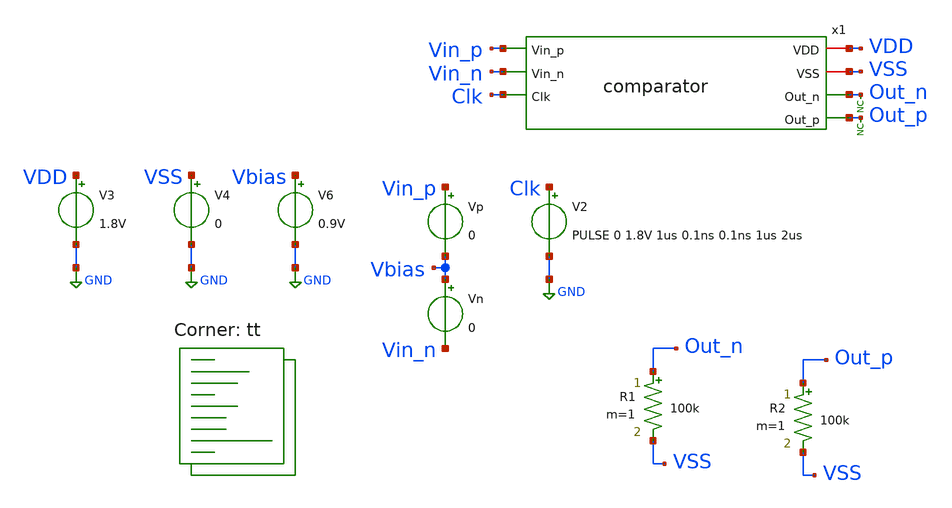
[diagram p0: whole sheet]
** sch_path: xschem/tests/comparator/comparator_stepped_test.sch
**.subckt comparator_stepped_test
V3 VDD GND 1.8V
V4 VSS GND 0
x1 VDD VSS Vin_p Out_n Vin_n Out_p Clk comparator
Vp Vin_p Vbias 0
V2 Clk GND PULSE 0 1.8V 1us 0.1ns 0.1ns 1us 2us
* noconn Out_p
* noconn Out_n
Vn Vbias Vin_n 0
V6 Vbias GND 0.9V
R1 Out_n VSS 100k m=1
R2 Out_p VSS 100k m=1
**** begin user architecture code
 *.lib $::SKYWATER_MODELS/sky130.lib.spice tt
.include $::SKYWATER_STDCELLS/sky130_fd_sc_hd.spice

.lib $::SKYWATER_MODELS/sky130.lib.spice tt



* ngspice commands
.control

* Go to the const plot
setplot const
save all

let vdiff = -0.005V
let vmax = 0.005V
let vdelta = 0.001;
let runs = 0

* Insert vector names and set only one scale
set wr_vecnames
set wr_singlescale
* Set the hardcopy plot type
set hcopydevtype=svg

let total_runs = ceil(($&vmax - $&vdiff) / $&vdelta)
let out_bits = vector($&total_runs*2)
let in_volts = vector($&total_runs)
reshape out_bits[2][$&total_runs]


while vdiff le $&vmax
	* Alter the voltages
	alter vp vdiff
	alter vn vdiff

	* Run the tran
	* tran creates a new plot starting with tran1
	tran 0.01u 3u

	* Measure the max to find the output
	meas tran p_max MAX v(out_p) from=0u to=3u
	meas tran n_max MAX v(out_n) from=0u to=3u

	set plotfile = plot{$&runs}.svg
	hardcopy $plotfile clk-4 vin_p-vin_n out_n+4 out_p+6

	* Create variables
	set p_max = $&p_max
	set n_max = $&n_max
	set vdiff = $&vdiff

	* Switch to constants plot
	setplot const
	*compose out_bits values $&out_bits $p_max $n_max
	let in_volts[$&runs] = $vdiff
	let out_bits[0][$&runs] = $p_max
	let out_bits[1][$&runs] = $n_max

	* set the iterators
	echo run $&runs
	let vdiff = vdiff + vdelta
	let runs = runs + 1

	* Destroy the transient plot to release memory
	destroy tran1

end

* switch to the const plot
setplot const
compose def_scale start=1 stop=$&total_runs step=1
setscale def_scale
echo Writing out_bits.txt
wrdata out_bits.txt in_volts out_bits

echo
echo Total Runs = $&runs
echo
.endc



**** end user architecture code
**.ends

* expanding   symbol:  src/comparator/comparator.sym # of pins=7
** sym_path: xschem/src/comparator/comparator.sym
** sch_path: xschem/src/comparator/comparator.sch
.subckt comparator VDD VSS Vin_p Out_n Vin_n Out_p Clk
*.iopin VDD
*.iopin VSS
*.ipin Vin_p
*.opin Out_n
*.ipin Vin_n
*.opin Out_p
*.ipin Clk
XM1 Pre_Amp_n Clk VDD VSS sky130_fd_pr__pfet_01v8 L=0.15 W=1 nf=1 ad='int((nf+1)/2) * W/nf * 0.29' as='int((nf+2)/2) * W/nf * 0.29'
+ pd='2*int((nf+1)/2) * (W/nf + 0.29)' ps='2*int((nf+2)/2) * (W/nf + 0.29)' nrd='0.29 / W' nrs='0.29 / W'
+ sa=0 sb=0 sd=0 mult=1 m=1
XM2 Pre_Amp_p Clk VDD VSS sky130_fd_pr__pfet_01v8 L=0.15 W=1 nf=1 ad='int((nf+1)/2) * W/nf * 0.29' as='int((nf+2)/2) * W/nf * 0.29'
+ pd='2*int((nf+1)/2) * (W/nf + 0.29)' ps='2*int((nf+2)/2) * (W/nf + 0.29)' nrd='0.29 / W' nrs='0.29 / W'
+ sa=0 sb=0 sd=0 mult=1 m=1
XM3 Pre_Amp_p Vin_p net1 VSS sky130_fd_pr__nfet_01v8 L=0.15 W=1 nf=1 ad='int((nf+1)/2) * W/nf * 0.29'
+ as='int((nf+2)/2) * W/nf * 0.29' pd='2*int((nf+1)/2) * (W/nf + 0.29)' ps='2*int((nf+2)/2) * (W/nf + 0.29)'
+ nrd='0.29 / W' nrs='0.29 / W' sa=0 sb=0 sd=0 mult=1 m=1
XM4 Pre_Amp_n Vin_n net1 VSS sky130_fd_pr__nfet_01v8 L=0.15 W=1 nf=1 ad='int((nf+1)/2) * W/nf * 0.29'
+ as='int((nf+2)/2) * W/nf * 0.29' pd='2*int((nf+1)/2) * (W/nf + 0.29)' ps='2*int((nf+2)/2) * (W/nf + 0.29)'
+ nrd='0.29 / W' nrs='0.29 / W' sa=0 sb=0 sd=0 mult=1 m=1
XM5 net3 Out_p VDD VSS sky130_fd_pr__pfet_01v8 L=0.15 W=1 nf=1 ad='int((nf+1)/2) * W/nf * 0.29' as='int((nf+2)/2) * W/nf * 0.29'
+ pd='2*int((nf+1)/2) * (W/nf + 0.29)' ps='2*int((nf+2)/2) * (W/nf + 0.29)' nrd='0.29 / W' nrs='0.29 / W'
+ sa=0 sb=0 sd=0 mult=1 m=1
XM6 net2 Out_n VDD VSS sky130_fd_pr__pfet_01v8 L=0.15 W=1 nf=1 ad='int((nf+1)/2) * W/nf * 0.29' as='int((nf+2)/2) * W/nf * 0.29'
+ pd='2*int((nf+1)/2) * (W/nf + 0.29)' ps='2*int((nf+2)/2) * (W/nf + 0.29)' nrd='0.29 / W' nrs='0.29 / W'
+ sa=0 sb=0 sd=0 mult=1 m=1
XM7 net2 Pre_Amp_p Out_p VSS sky130_fd_pr__nfet_01v8 L=0.15 W=1 nf=1 ad='int((nf+1)/2) * W/nf * 0.29'
+ as='int((nf+2)/2) * W/nf * 0.29' pd='2*int((nf+1)/2) * (W/nf + 0.29)' ps='2*int((nf+2)/2) * (W/nf + 0.29)'
+ nrd='0.29 / W' nrs='0.29 / W' sa=0 sb=0 sd=0 mult=1 m=1
XM8 net3 Pre_Amp_n Out_n VSS sky130_fd_pr__nfet_01v8 L=0.15 W=1 nf=1 ad='int((nf+1)/2) * W/nf * 0.29'
+ as='int((nf+2)/2) * W/nf * 0.29' pd='2*int((nf+1)/2) * (W/nf + 0.29)' ps='2*int((nf+2)/2) * (W/nf + 0.29)'
+ nrd='0.29 / W' nrs='0.29 / W' sa=0 sb=0 sd=0 mult=1 m=1
XM9 net1 Clk VSS VSS sky130_fd_pr__nfet_01v8 L=0.15 W=1 nf=1 ad='int((nf+1)/2) * W/nf * 0.29' as='int((nf+2)/2) * W/nf * 0.29'
+ pd='2*int((nf+1)/2) * (W/nf + 0.29)' ps='2*int((nf+2)/2) * (W/nf + 0.29)' nrd='0.29 / W' nrs='0.29 / W'
+ sa=0 sb=0 sd=0 mult=1 m=1
XM10 Pre_Amp_n Vin_n net1 VSS sky130_fd_pr__nfet_01v8 L=0.15 W=1 nf=1 ad='int((nf+1)/2) * W/nf * 0.29'
+ as='int((nf+2)/2) * W/nf * 0.29' pd='2*int((nf+1)/2) * (W/nf + 0.29)' ps='2*int((nf+2)/2) * (W/nf + 0.29)'
+ nrd='0.29 / W' nrs='0.29 / W' sa=0 sb=0 sd=0 mult=1 m=1
XM11 Out_n Clk_n VSS VSS sky130_fd_pr__nfet_01v8 L=0.15 W=1 nf=1 ad='int((nf+1)/2) * W/nf * 0.29' as='int((nf+2)/2) * W/nf * 0.29'
+ pd='2*int((nf+1)/2) * (W/nf + 0.29)' ps='2*int((nf+2)/2) * (W/nf + 0.29)' nrd='0.29 / W' nrs='0.29 / W'
+ sa=0 sb=0 sd=0 mult=1 m=1
XM12 Out_n Out_p VSS VSS sky130_fd_pr__nfet_01v8 L=0.15 W=1 nf=1 ad='int((nf+1)/2) * W/nf * 0.29' as='int((nf+2)/2) * W/nf * 0.29'
+ pd='2*int((nf+1)/2) * (W/nf + 0.29)' ps='2*int((nf+2)/2) * (W/nf + 0.29)' nrd='0.29 / W' nrs='0.29 / W'
+ sa=0 sb=0 sd=0 mult=1 m=1
XM13 Out_p Out_n VSS VSS sky130_fd_pr__nfet_01v8 L=0.15 W=1 nf=1 ad='int((nf+1)/2) * W/nf * 0.29' as='int((nf+2)/2) * W/nf * 0.29'
+ pd='2*int((nf+1)/2) * (W/nf + 0.29)' ps='2*int((nf+2)/2) * (W/nf + 0.29)' nrd='0.29 / W' nrs='0.29 / W'
+ sa=0 sb=0 sd=0 mult=1 m=1
XM14 Out_p Clk_n VSS VSS sky130_fd_pr__nfet_01v8 L=0.15 W=1 nf=1 ad='int((nf+1)/2) * W/nf * 0.29' as='int((nf+2)/2) * W/nf * 0.29'
+ pd='2*int((nf+1)/2) * (W/nf + 0.29)' ps='2*int((nf+2)/2) * (W/nf + 0.29)' nrd='0.29 / W' nrs='0.29 / W'
+ sa=0 sb=0 sd=0 mult=1 m=1
XM15 Clk_n Clk VDD VSS sky130_fd_pr__pfet_01v8 L=0.15 W=1 nf=1 ad='int((nf+1)/2) * W/nf * 0.29' as='int((nf+2)/2) * W/nf * 0.29'
+ pd='2*int((nf+1)/2) * (W/nf + 0.29)' ps='2*int((nf+2)/2) * (W/nf + 0.29)' nrd='0.29 / W' nrs='0.29 / W'
+ sa=0 sb=0 sd=0 mult=1 m=1
XM16 Clk_n Clk VSS VSS sky130_fd_pr__nfet_01v8 L=0.15 W=1 nf=1 ad='int((nf+1)/2) * W/nf * 0.29' as='int((nf+2)/2) * W/nf * 0.29'
+ pd='2*int((nf+1)/2) * (W/nf + 0.29)' ps='2*int((nf+2)/2) * (W/nf + 0.29)' nrd='0.29 / W' nrs='0.29 / W'
+ sa=0 sb=0 sd=0 mult=1 m=1
.ends

.GLOBAL GND
.end
